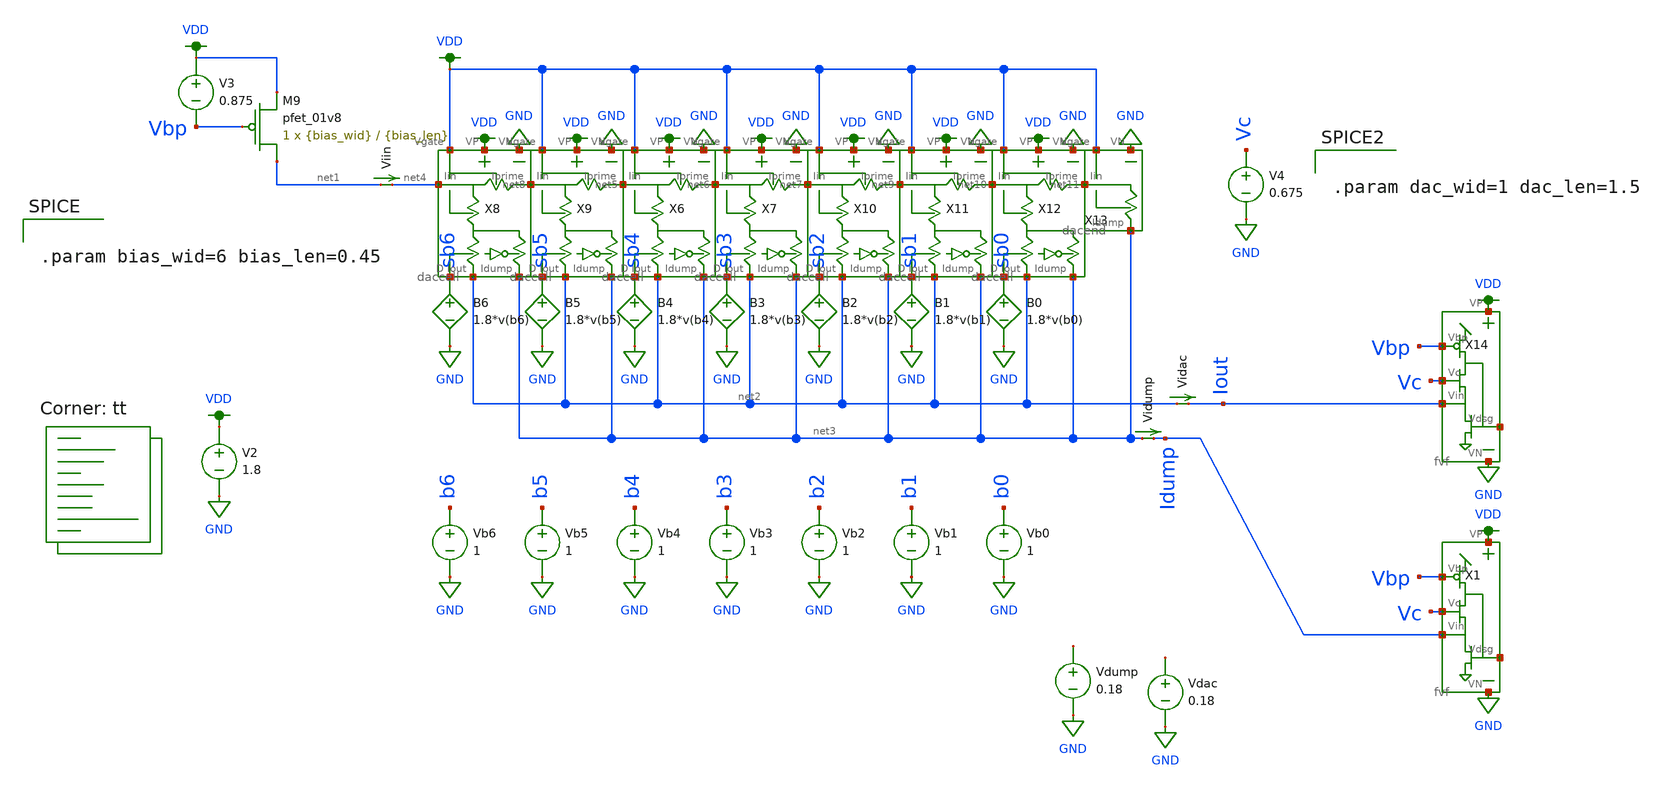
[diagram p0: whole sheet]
** sch_path: test_dac_2.sch
**.subckt test_dac_2
V2 VDD GND 1.8
X6 sb4 net3 VDD GND net2 net5 net6 VDD daccell
X7 sb3 net3 VDD GND net2 net6 net7 VDD daccell
X8 sb6 net3 VDD GND net2 net4 net8 VDD daccell
X9 sb5 net3 VDD GND net2 net8 net5 VDD daccell
X10 sb2 net3 VDD GND net2 net7 net9 VDD daccell
X11 sb1 net3 VDD GND net2 net9 net10 VDD daccell
X12 sb0 net3 VDD GND net2 net10 net11 VDD daccell
X13 net3 GND net11 VDD dacend
XM9 net1 Vbp VDD VP sky130_fd_pr__pfet_01v8 L={bias_len} W={bias_wid} nf=1 ad='int((nf+1)/2) * W/nf * 0.29'
+ as='int((nf+2)/2) * W/nf * 0.29' pd='2*int((nf+1)/2) * (W/nf + 0.29)' ps='2*int((nf+2)/2) * (W/nf + 0.29)'
+ nrd='0.29 / W' nrs='0.29 / W' sa=0 sb=0 sd=0 mult=1 m=1
Vb0 b0 GND 1
Viin net1 net4 0
.save i(viin)
B0 sb0 GND V=1.8*v(b0)
Vb1 b1 GND 1
B1 sb1 GND V=1.8*v(b1)
Vb2 b2 GND 1
B2 sb2 GND V=1.8*v(b2)
Vb3 b3 GND 1
B3 sb3 GND V=1.8*v(b3)
Vb4 b4 GND 1
B4 sb4 GND V=1.8*v(b4)
Vb5 b5 GND 1
B5 sb5 GND V=1.8*v(b5)
Vb6 b6 GND 1
B6 sb6 GND V=1.8*v(b6)
Vidump net3 Idump 0
.save i(vidump)
V3 VDD Vbp 0.875
Vidac net2 Iout 0
.save i(vidac)
Vdump net12 GND 0.18
Vdac net13 GND 0.18
X14 VDD Vbp Vc Iout net14 GND fvf
V4 Vc GND 0.675
X1 VDD Vbp Vc Idump net15 GND fvf
**** begin user architecture code
.lib $::SKYWATER_MODELS/sky130.lib.spice tt


.control
  set wr_vecnames
  set wr_singlescale
  let code = 0
  while code < 128
    if code eq 0
      let b0 = 0
    else
      let b0 = code % 2
    end
    if floor(code / 2) eq 0
      let b1 = 0
    else
      let b1 = floor(code / 2) % 2
    end
    if floor(code / 4) eq 0
      let b2 = 0
    else
      let b2 = floor(code / 4) % 2
    end
    if floor(code / 8) eq 0
      let b3 = 0
    else
      let b3 = floor(code / 8) % 2
    end
    if floor(code / 16) eq 0
      let b4 = 0
    else
      let b4 = floor(code / 16) % 2
    end
    if floor(code / 32) eq 0
      let b5 = 0
    else
      let b5 = floor(code / 32) % 2
    end
    if floor(code / 64) eq 0
      let b6 = 0
    else
      let b6 = floor(code / 64) % 2
    end
    alter vb0 $&b0
    alter vb1 $&b1
    alter vb2 $&b2
    alter vb3 $&b3
    alter vb4 $&b4
    alter vb5 $&b5
    alter vb6 $&b6
    save all
    op
    wrdata ~/Documents/mosfet-dac/test_dac.txt code v(sb0) v(sb1) v(sb2) v(sb3) v(sb4) v(sb5) v(sb6)
+ i(Viin) i(Vidac) i(Vidump) v(Iout) v(Idump)
    if code eq 0
      set appendwrite
      set wr_vecnames = FALSE
    end
    let code = code + 1
  end
  quit
.endc



.param bias_wid=6 bias_len=0.45




.param dac_wid=1 dac_len=1.5


**** end user architecture code
**.ends
.GLOBAL GND
.GLOBAL VDD
.end
